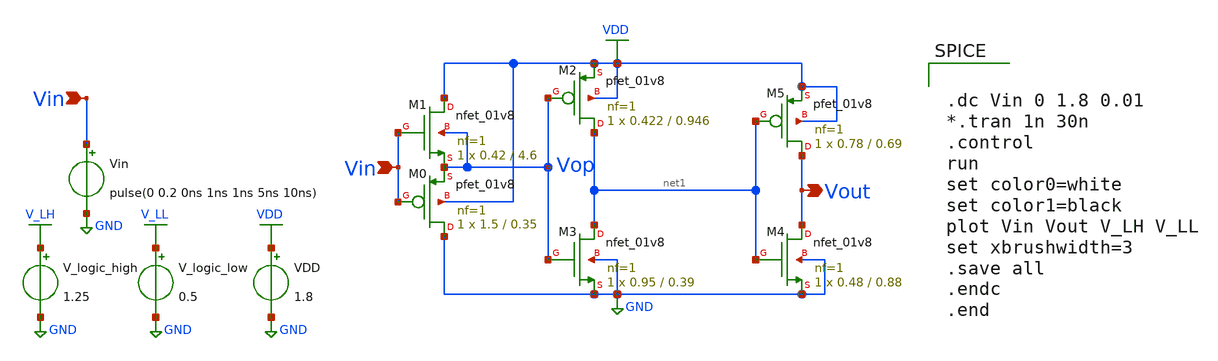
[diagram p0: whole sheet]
** sch_path: xschem/Vth_sch/th01.sch
**.subckt th01 Vin Vin Vout
*.ipin Vin
*.ipin Vin
*.opin Vout
VDD VDD GND 1.8
Vin Vin GND pulse(0 0.2 0ns 1ns 1ns 5ns 10ns)
V_logic_high V_LH GND 1.25
V_logic_low V_LL GND 0.5
XM5 Vout net1 VDD VDD sky130_fd_pr__pfet_01v8 L=0.69 W=0.78 nf=1 ad='int((nf+1)/2) * W/nf * 0.29' as='int((nf+2)/2) * W/nf * 0.29'
+ pd='2*int((nf+1)/2) * (W/nf + 0.29)' ps='2*int((nf+2)/2) * (W/nf + 0.29)' nrd='0.29 / W' nrs='0.29 / W'
+ sa=0 sb=0 sd=0 mult=1 m=1
XM4 Vout net1 GND GND sky130_fd_pr__nfet_01v8 L=0.88 W=0.48 nf=1 ad='int((nf+1)/2) * W/nf * 0.29' as='int((nf+2)/2) * W/nf * 0.29'
+ pd='2*int((nf+1)/2) * (W/nf + 0.29)' ps='2*int((nf+2)/2) * (W/nf + 0.29)' nrd='0.29 / W' nrs='0.29 / W'
+ sa=0 sb=0 sd=0 mult=1 m=1
XM2 net1 Vop VDD VDD sky130_fd_pr__pfet_01v8 L=0.946 W=0.422 nf=1 ad='int((nf+1)/2) * W/nf * 0.29' as='int((nf+2)/2) * W/nf * 0.29'
+ pd='2*int((nf+1)/2) * (W/nf + 0.29)' ps='2*int((nf+2)/2) * (W/nf + 0.29)' nrd='0.29 / W' nrs='0.29 / W'
+ sa=0 sb=0 sd=0 mult=1 m=1
XM3 net1 Vop GND GND sky130_fd_pr__nfet_01v8 L=0.39 W=0.95 nf=1 ad='int((nf+1)/2) * W/nf * 0.29' as='int((nf+2)/2) * W/nf * 0.29'
+ pd='2*int((nf+1)/2) * (W/nf + 0.29)' ps='2*int((nf+2)/2) * (W/nf + 0.29)' nrd='0.29 / W' nrs='0.29 / W'
+ sa=0 sb=0 sd=0 mult=1 m=1
XM1 VDD Vin Vop Vop sky130_fd_pr__nfet_01v8 L=4.6 W=0.42 nf=1 ad='int((nf+1)/2) * W/nf * 0.29' as='int((nf+2)/2) * W/nf * 0.29'
+ pd='2*int((nf+1)/2) * (W/nf + 0.29)' ps='2*int((nf+2)/2) * (W/nf + 0.29)' nrd='0.29 / W' nrs='0.29 / W'
+ sa=0 sb=0 sd=0 mult=1 m=1
XM0 GND Vin Vop VDD sky130_fd_pr__pfet_01v8 L=0.35 W=1.5 nf=1 ad='int((nf+1)/2) * W/nf * 0.29' as='int((nf+2)/2) * W/nf * 0.29'
+ pd='2*int((nf+1)/2) * (W/nf + 0.29)' ps='2*int((nf+2)/2) * (W/nf + 0.29)' nrd='0.29 / W' nrs='0.29 / W'
+ sa=0 sb=0 sd=0 mult=1 m=1
**** begin user architecture code


.lib /usr/local/share/pdk/sky130A/libs.tech/ngspice/sky130.lib.spice tt

.save all





.dc Vin 0 1.8 0.01
*.tran 1n 30n
.control
run
set color0=white
set color1=black
plot Vin Vout V_LH V_LL
set xbrushwidth=3
.save all
.endc
.end


**** end user architecture code
**.ends
.GLOBAL VDD
.GLOBAL GND
.GLOBAL V_LH
.GLOBAL V_LL
.end
